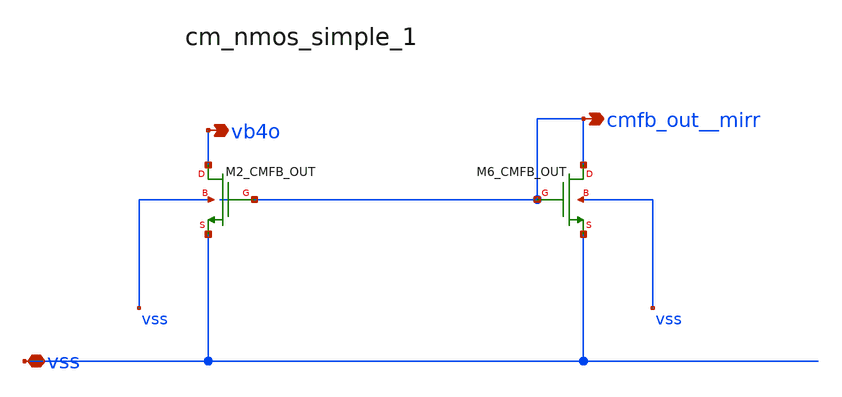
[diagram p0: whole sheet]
** sch_path: analog-db/raw/amp_035_fan_chopper_cmfb_dual/hier/blocks/cm_nmos_simple_1.sch
**.subckt cm_nmos_simple_1 vss vb4o cmfb_out__mirr
*.iopin vss
*.opin vb4o
*.opin cmfb_out__mirr
XM2_CMFB_OUT vb4o cmfb_out__mirr vss vss sg13_lv_nmos w=x_dut_xm2_cmfb_out_w l=x_dut_xm2_cmfb_out_l
+ ng=1 m=x_dut_xm2_cmfb_out_m
XM6_CMFB_OUT cmfb_out__mirr cmfb_out__mirr vss vss sg13_lv_nmos w=x_dut_xm6_cmfb_out_w
+ l=x_dut_xm6_cmfb_out_l ng=1 m=x_dut_xm6_cmfb_out_m
**.ends
.end
